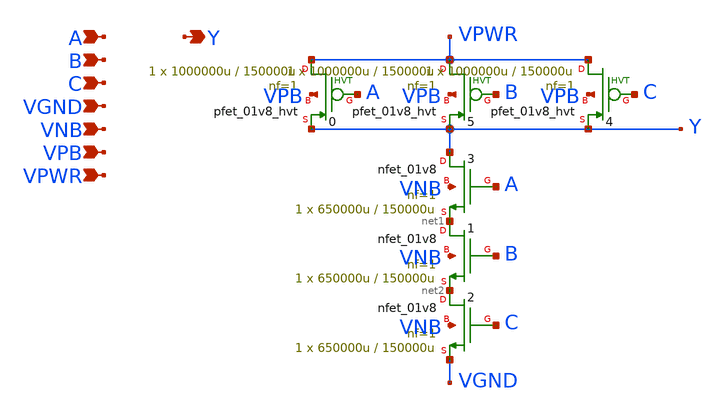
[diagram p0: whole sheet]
** sch_path: schematics/nand3/sky130_fd_sc_hd__nand3_1.sch
**.subckt sky130_fd_sc_hd__nand3_1 A B C VGND VNB VPB VPWR Y
*.ipin A
*.ipin B
*.ipin C
*.ipin VGND
*.ipin VNB
*.ipin VPB
*.ipin VPWR
*.opin Y
X5 VPWR B Y VPB sky130_fd_pr__pfet_01v8_hvt L=150000u W=1000000u nf=1 ad='int((1 + 1)/2) * 1000000u / 1 * 0.29'
+ as='int((1 + 2)/2) * 1000000u / 1 * 0.29' pd='2*int((1 + 1)/2) * (1000000u / 1 + 0.29)' ps='2*int((1 + 2)/2) * (1000000u / 1 + 0.29)'
+ nrd='0.29 / 1000000u ' nrs='0.29 / 1000000u ' sa=0 sb=0 sd=0 mult=1 m=1
X0 VPWR A Y VPB sky130_fd_pr__pfet_01v8_hvt L=150000u W=1000000u nf=1 ad='int((1 + 1)/2) * 1000000u / 1 * 0.29'
+ as='int((1 + 2)/2) * 1000000u / 1 * 0.29' pd='2*int((1 + 1)/2) * (1000000u / 1 + 0.29)' ps='2*int((1 + 2)/2) * (1000000u / 1 + 0.29)'
+ nrd='0.29 / 1000000u ' nrs='0.29 / 1000000u ' sa=0 sb=0 sd=0 mult=1 m=1
X3 Y A net1 VNB sky130_fd_pr__nfet_01v8 L=150000u W=650000u nf=1 ad='int((1 + 1)/2) * 650000u / 1 * 0.29'
+ as='int((1 + 2)/2) * 650000u / 1 * 0.29' pd='2*int((1 + 1)/2) * (650000u / 1 + 0.29)' ps='2*int((1 + 2)/2) * (650000u / 1 + 0.29)'
+ nrd='0.29 / 650000u ' nrs='0.29 / 650000u ' sa=0 sb=0 sd=0 mult=1 m=1
X1 net1 B net2 VNB sky130_fd_pr__nfet_01v8 L=150000u W=650000u nf=1 ad='int((1 + 1)/2) * 650000u / 1 * 0.29'
+ as='int((1 + 2)/2) * 650000u / 1 * 0.29' pd='2*int((1 + 1)/2) * (650000u / 1 + 0.29)' ps='2*int((1 + 2)/2) * (650000u / 1 + 0.29)'
+ nrd='0.29 / 650000u ' nrs='0.29 / 650000u ' sa=0 sb=0 sd=0 mult=1 m=1
X4 VPWR C Y VPB sky130_fd_pr__pfet_01v8_hvt L=150000u W=1000000u nf=1 ad='int((1 + 1)/2) * 1000000u / 1 * 0.29'
+ as='int((1 + 2)/2) * 1000000u / 1 * 0.29' pd='2*int((1 + 1)/2) * (1000000u / 1 + 0.29)' ps='2*int((1 + 2)/2) * (1000000u / 1 + 0.29)'
+ nrd='0.29 / 1000000u ' nrs='0.29 / 1000000u ' sa=0 sb=0 sd=0 mult=1 m=1
X2 net2 C VGND VNB sky130_fd_pr__nfet_01v8 L=150000u W=650000u nf=1 ad='int((1 + 1)/2) * 650000u / 1 * 0.29'
+ as='int((1 + 2)/2) * 650000u / 1 * 0.29' pd='2*int((1 + 1)/2) * (650000u / 1 + 0.29)' ps='2*int((1 + 2)/2) * (650000u / 1 + 0.29)'
+ nrd='0.29 / 650000u ' nrs='0.29 / 650000u ' sa=0 sb=0 sd=0 mult=1 m=1
**.ends
.end
